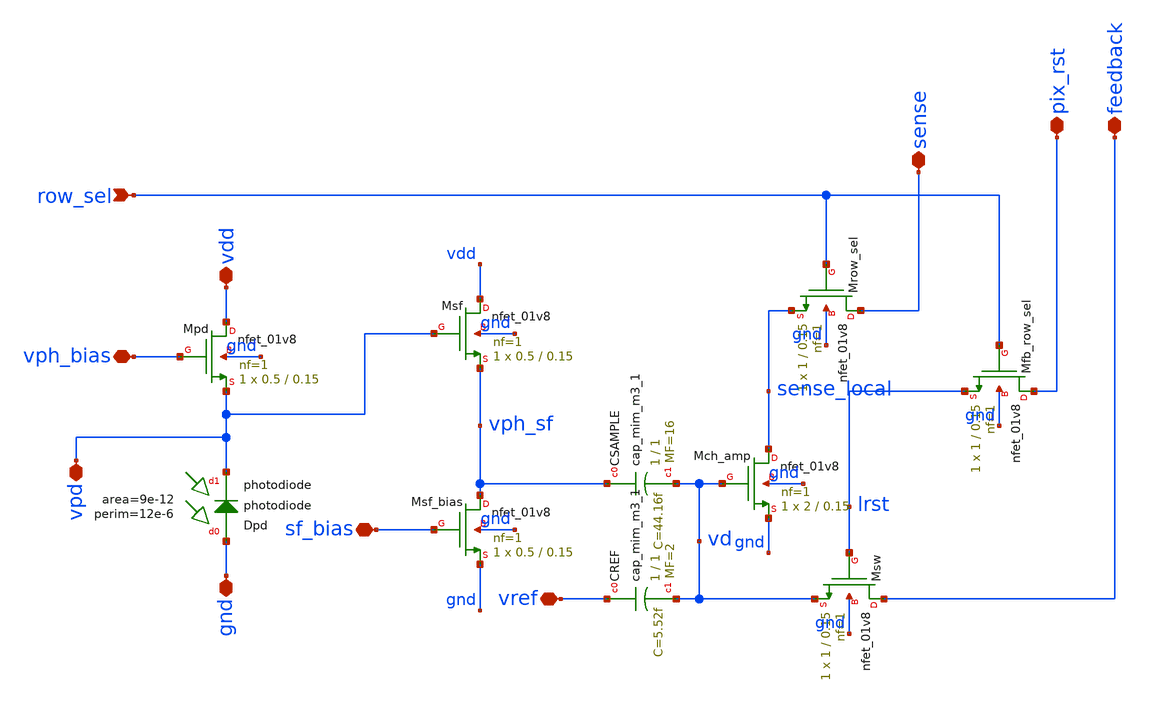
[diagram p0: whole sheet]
** sch_path: analog/xschem/openDVS_pixel.sch
**.subckt openDVS_pixel row_sel sense pix_rst feedback vph_bias vdd vref vpd sf_bias gnd
*.ipin row_sel
*.iopin sense
*.iopin pix_rst
*.iopin feedback
*.iopin vph_bias
*.iopin vdd
*.iopin vref
*.iopin vpd
*.iopin sf_bias
*.iopin gnd
XCSAMPLE vph_sf vd sky130_fd_pr__cap_mim_m3_1 W=1 L=1 MF=16 m=16
XCREF vref vd sky130_fd_pr__cap_mim_m3_1 W=1 L=1 MF=2 m=2
XMpd vdd vph_bias vpd gnd sky130_fd_pr__nfet_01v8 L=0.15 W=0.5 nf=1 ad='int((1 + 1)/2) * 0.5 / 1 * 0.29'
+ as='int((1 + 2)/2) * 0.5 / 1 * 0.29' pd='2*int((1 + 1)/2) * (0.5 / 1 + 0.29)' ps='2*int((1 + 2)/2) * (0.5 / 1 + 0.29)'
+ nrd='0.29 / 0.5 ' nrs='0.29 / 0.5 ' sa=0 sb=0 sd=0 mult=1 m=1
XMch_amp sense_local vd gnd gnd sky130_fd_pr__nfet_01v8 L=0.15 W=2 nf=1 ad='int((1 + 1)/2) * 2 / 1 * 0.29'
+ as='int((1 + 2)/2) * 2 / 1 * 0.29' pd='2*int((1 + 1)/2) * (2 / 1 + 0.29)' ps='2*int((1 + 2)/2) * (2 / 1 + 0.29)'
+ nrd='0.29 / 2 ' nrs='0.29 / 2 ' sa=0 sb=0 sd=0 mult=1 m=1
XMsw feedback lrst vd gnd sky130_fd_pr__nfet_01v8 L=0.15 W=1 nf=1 ad='int((1 + 1)/2) * 1 / 1 * 0.29'
+ as='int((1 + 2)/2) * 1 / 1 * 0.29' pd='2*int((1 + 1)/2) * (1 / 1 + 0.29)' ps='2*int((1 + 2)/2) * (1 / 1 + 0.29)'
+ nrd='0.29 / 1 ' nrs='0.29 / 1 ' sa=0 sb=0 sd=0 mult=1 m=1
XMsf_bias vph_sf sf_bias gnd gnd sky130_fd_pr__nfet_01v8 L=0.15 W=0.5 nf=1 ad='int((1 + 1)/2) * 0.5 / 1 * 0.29'
+ as='int((1 + 2)/2) * 0.5 / 1 * 0.29' pd='2*int((1 + 1)/2) * (0.5 / 1 + 0.29)' ps='2*int((1 + 2)/2) * (0.5 / 1 + 0.29)'
+ nrd='0.29 / 0.5 ' nrs='0.29 / 0.5 ' sa=0 sb=0 sd=0 mult=1 m=1
XMsf vdd vpd vph_sf gnd sky130_fd_pr__nfet_01v8 L=0.15 W=0.5 nf=1 ad='int((1 + 1)/2) * 0.5 / 1 * 0.29'
+ as='int((1 + 2)/2) * 0.5 / 1 * 0.29' pd='2*int((1 + 1)/2) * (0.5 / 1 + 0.29)' ps='2*int((1 + 2)/2) * (0.5 / 1 + 0.29)'
+ nrd='0.29 / 0.5 ' nrs='0.29 / 0.5 ' sa=0 sb=0 sd=0 mult=1 m=1
XMrow_sel sense row_sel sense_local gnd sky130_fd_pr__nfet_01v8 L=0.15 W=1 nf=1 ad='int((1 + 1)/2) * 1 / 1 * 0.29'
+ as='int((1 + 2)/2) * 1 / 1 * 0.29' pd='2*int((1 + 1)/2) * (1 / 1 + 0.29)' ps='2*int((1 + 2)/2) * (1 / 1 + 0.29)'
+ nrd='0.29 / 1 ' nrs='0.29 / 1 ' sa=0 sb=0 sd=0 mult=1 m=1
XMfb_row_sel pix_rst row_sel lrst gnd sky130_fd_pr__nfet_01v8 L=0.15 W=1 nf=1 ad='int((1 + 1)/2) * 1 / 1 * 0.29'
+ as='int((1 + 2)/2) * 1 / 1 * 0.29' pd='2*int((1 + 1)/2) * (1 / 1 + 0.29)' ps='2*int((1 + 2)/2) * (1 / 1 + 0.29)'
+ nrd='0.29 / 1 ' nrs='0.29 / 1 ' sa=0 sb=0 sd=0 mult=1 m=1
XDpd gnd vpd sky130_fd_pr__photodiode area=9e-12 perim=12e-6
**.ends
.end
